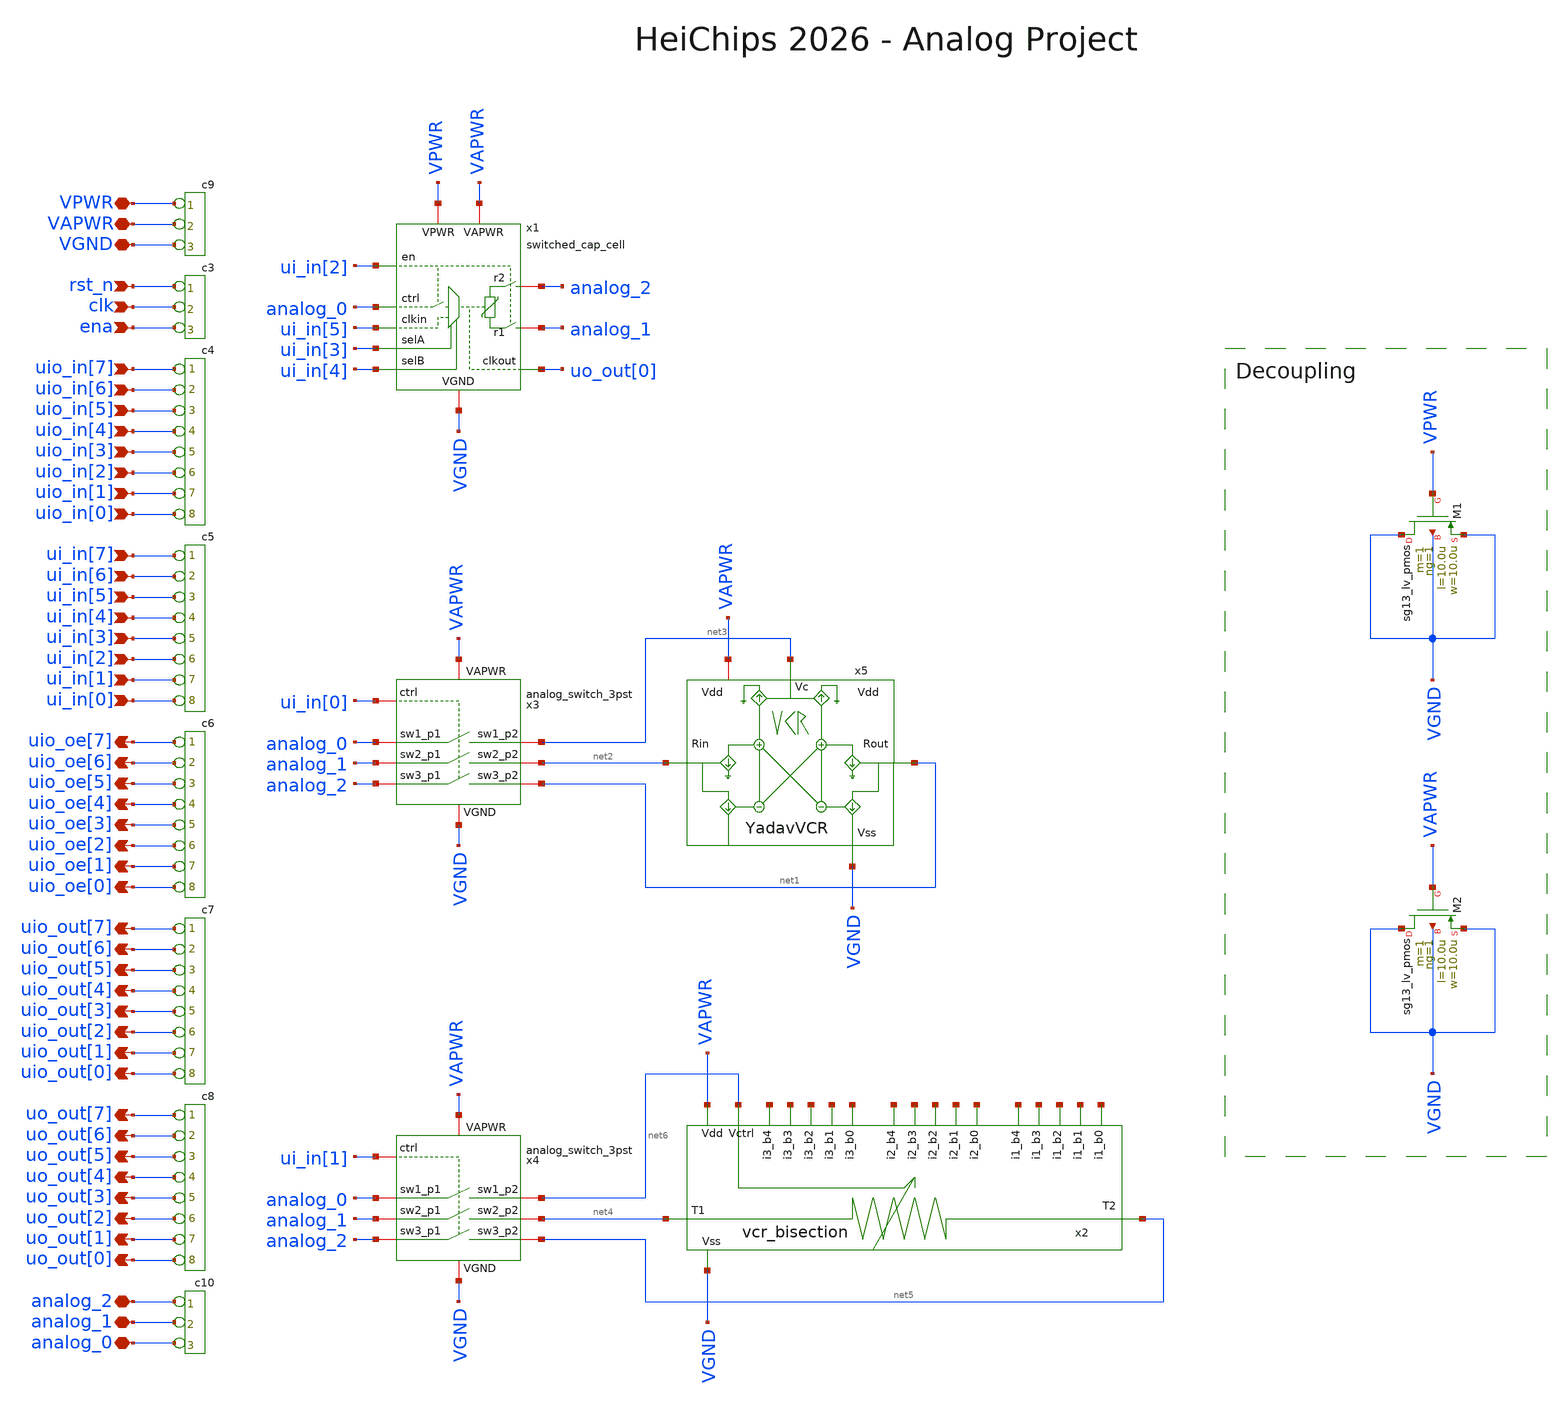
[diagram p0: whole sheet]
** sch_path: macros/heichips26_vcr/schematic/xschem/heichips26_analog_project.sch
**.subckt heichips26_analog_project rst_n clk ena uio_in[7] ui_in[7] uio_oe[7] uio_oe[6] uio_oe[5]
*+ uio_oe[4] uio_oe[3] uio_oe[2] uio_oe[1] uio_oe[0] uio_out[7] uio_out[6] uio_out[5] uio_out[4] uio_out[3]
*+ uio_out[2] uio_out[1] uio_out[0] uo_out[7] uo_out[6] uo_out[5] uo_out[4] uo_out[3] uo_out[2] uo_out[1]
*+ uo_out[0] VPWR VGND VAPWR ui_in[6] ui_in[5] ui_in[4] ui_in[3] ui_in[2] ui_in[1] ui_in[0] uio_in[6] uio_in[5]
*+ uio_in[4] uio_in[3] uio_in[2] uio_in[1] uio_in[0] analog_2 analog_1 analog_0
*.ipin rst_n
*.ipin clk
*.ipin ena
*.ipin uio_in[7]
*.ipin ui_in[7]
*.opin uio_oe[7]
*.opin uio_oe[6]
*.opin uio_oe[5]
*.opin uio_oe[4]
*.opin uio_oe[3]
*.opin uio_oe[2]
*.opin uio_oe[1]
*.opin uio_oe[0]
*.opin uio_out[7]
*.opin uio_out[6]
*.opin uio_out[5]
*.opin uio_out[4]
*.opin uio_out[3]
*.opin uio_out[2]
*.opin uio_out[1]
*.opin uio_out[0]
*.opin uo_out[7]
*.opin uo_out[6]
*.opin uo_out[5]
*.opin uo_out[4]
*.opin uo_out[3]
*.opin uo_out[2]
*.opin uo_out[1]
*.opin uo_out[0]
*.iopin VPWR
*.iopin VGND
*.iopin VAPWR
*.ipin ui_in[6]
*.ipin ui_in[5]
*.ipin ui_in[4]
*.ipin ui_in[3]
*.ipin ui_in[2]
*.ipin ui_in[1]
*.ipin ui_in[0]
*.ipin uio_in[6]
*.ipin uio_in[5]
*.ipin uio_in[4]
*.ipin uio_in[3]
*.ipin uio_in[2]
*.ipin uio_in[1]
*.ipin uio_in[0]
*.iopin analog_2
*.iopin analog_1
*.iopin analog_0
*connector(3,1) ?1 rst_n ?1 clk ?1 ena
*connector(8,1) ?1 uio_in[7] ?1 uio_in[6] ?1 uio_in[5] ?1 uio_in[4] ?1 uio_in[3] ?1 uio_in[2] ?1
*+ uio_in[1] ?1 uio_in[0]
*connector(8,1) ?1 ui_in[7] ?1 ui_in[6] ?1 ui_in[5] ?1 ui_in[4] ?1 ui_in[3] ?1 ui_in[2] ?1 ui_in[1]
*+ ?1 ui_in[0]
*connector(8,1) ?1 uio_oe[7] ?1 uio_oe[6] ?1 uio_oe[5] ?1 uio_oe[4] ?1 uio_oe[3] ?1 uio_oe[2] ?1
*+ uio_oe[1] ?1 uio_oe[0]
*connector(8,1) ?1 uio_out[7] ?1 uio_out[6] ?1 uio_out[5] ?1 uio_out[4] ?1 uio_out[3] ?1 uio_out[2]
*+ ?1 uio_out[1] ?1 uio_out[0]
*connector(8,1) ?1 uo_out[7] ?1 uo_out[6] ?1 uo_out[5] ?1 uo_out[4] ?1 uo_out[3] ?1 uo_out[2] ?1
*+ uo_out[1] ?1 uo_out[0]
*connector(3,1) ?1 VPWR ?1 VAPWR ?1 VGND
*connector(3,1) ?1 analog_2 ?1 analog_1 ?1 analog_0
XM1 VGND VPWR VGND VGND sg13_lv_pmos w=10.0u l=10.0u ng=1 m=1 mm_ok=1
XM2 VGND VAPWR VGND VGND sg13_lv_pmos w=10.0u l=10.0u ng=1 m=1 mm_ok=1
x1 analog_0 VAPWR VGND analog_2 analog_1 ui_in[5] ui_in[3] ui_in[4] ui_in[2] VPWR uo_out[0]
+ switched_cap_cell
x2 net7 net8 net9 net10 net11 net12 net13 net14 net15 net16 net17 net18 net19 net20 net21 net6 VAPWR
+ VGND net5 net4 vcr_bisection
x5 VAPWR net2 net1 net3 VGND YadavVCR
x3 net3 analog_0 VAPWR ui_in[0] VGND net2 analog_1 net1 analog_2 analog_switch_3pst
x4 net6 analog_0 VAPWR ui_in[1] VGND net4 analog_1 net5 analog_2 analog_switch_3pst
**.ends
.end
